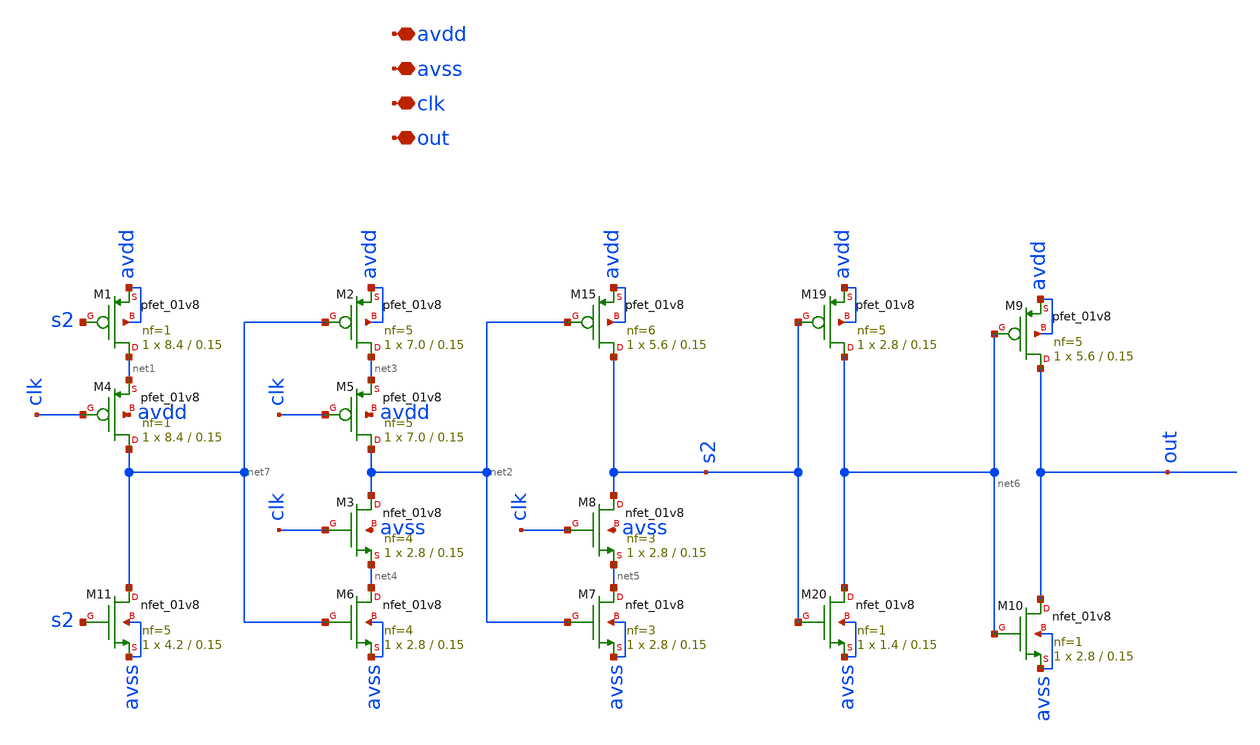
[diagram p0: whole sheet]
** sch_path: xschem/d_ff_2.sch
**.subckt d_ff_2 avdd avss clk out
*.iopin avdd
*.iopin avss
*.iopin clk
*.iopin out
XM4 net7 clk net1 avdd sky130_fd_pr__pfet_01v8 L=0.15 W=8.4 nf=1 ad='int((nf+1)/2) * W/nf * 0.29' as='int((nf+2)/2) * W/nf * 0.29'
+ pd='2*int((nf+1)/2) * (W/nf + 0.29)' ps='2*int((nf+2)/2) * (W/nf + 0.29)' nrd='0.29 / W' nrs='0.29 / W'
+ sa=0 sb=0 sd=0 mult=1 m=1
XM1 net1 s2 avdd avdd sky130_fd_pr__pfet_01v8 L=0.15 W=8.4 nf=1 ad='int((nf+1)/2) * W/nf * 0.29' as='int((nf+2)/2) * W/nf * 0.29'
+ pd='2*int((nf+1)/2) * (W/nf + 0.29)' ps='2*int((nf+2)/2) * (W/nf + 0.29)' nrd='0.29 / W' nrs='0.29 / W'
+ sa=0 sb=0 sd=0 mult=1 m=1
XM11 net7 s2 avss avss sky130_fd_pr__nfet_01v8 L=0.15 W=4.2 nf=5 ad='int((nf+1)/2) * W/nf * 0.29' as='int((nf+2)/2) * W/nf * 0.29'
+ pd='2*int((nf+1)/2) * (W/nf + 0.29)' ps='2*int((nf+2)/2) * (W/nf + 0.29)' nrd='0.29 / W' nrs='0.29 / W'
+ sa=0 sb=0 sd=0 mult=1 m=1
XM3 net2 clk net4 avss sky130_fd_pr__nfet_01v8 L=0.15 W=2.8 nf=4 ad='int((nf+1)/2) * W/nf * 0.29' as='int((nf+2)/2) * W/nf * 0.29'
+ pd='2*int((nf+1)/2) * (W/nf + 0.29)' ps='2*int((nf+2)/2) * (W/nf + 0.29)' nrd='0.29 / W' nrs='0.29 / W'
+ sa=0 sb=0 sd=0 mult=1 m=1
XM5 net2 clk net3 avdd sky130_fd_pr__pfet_01v8 L=0.15 W=7.0 nf=5 ad='int((nf+1)/2) * W/nf * 0.29' as='int((nf+2)/2) * W/nf * 0.29'
+ pd='2*int((nf+1)/2) * (W/nf + 0.29)' ps='2*int((nf+2)/2) * (W/nf + 0.29)' nrd='0.29 / W' nrs='0.29 / W'
+ sa=0 sb=0 sd=0 mult=1 m=1
XM2 net3 net7 avdd avdd sky130_fd_pr__pfet_01v8 L=0.15 W=7.0 nf=5 ad='int((nf+1)/2) * W/nf * 0.29' as='int((nf+2)/2) * W/nf * 0.29'
+ pd='2*int((nf+1)/2) * (W/nf + 0.29)' ps='2*int((nf+2)/2) * (W/nf + 0.29)' nrd='0.29 / W' nrs='0.29 / W'
+ sa=0 sb=0 sd=0 mult=1 m=1
XM6 net4 net7 avss avss sky130_fd_pr__nfet_01v8 L=0.15 W=2.8 nf=4 ad='int((nf+1)/2) * W/nf * 0.29' as='int((nf+2)/2) * W/nf * 0.29'
+ pd='2*int((nf+1)/2) * (W/nf + 0.29)' ps='2*int((nf+2)/2) * (W/nf + 0.29)' nrd='0.29 / W' nrs='0.29 / W'
+ sa=0 sb=0 sd=0 mult=1 m=1
XM8 s2 clk net5 avss sky130_fd_pr__nfet_01v8 L=0.15 W=2.8 nf=3 ad='int((nf+1)/2) * W/nf * 0.29' as='int((nf+2)/2) * W/nf * 0.29'
+ pd='2*int((nf+1)/2) * (W/nf + 0.29)' ps='2*int((nf+2)/2) * (W/nf + 0.29)' nrd='0.29 / W' nrs='0.29 / W'
+ sa=0 sb=0 sd=0 mult=1 m=1
XM15 s2 net2 avdd avdd sky130_fd_pr__pfet_01v8 L=0.15 W=5.6 nf=6 ad='int((nf+1)/2) * W/nf * 0.29' as='int((nf+2)/2) * W/nf * 0.29'
+ pd='2*int((nf+1)/2) * (W/nf + 0.29)' ps='2*int((nf+2)/2) * (W/nf + 0.29)' nrd='0.29 / W' nrs='0.29 / W'
+ sa=0 sb=0 sd=0 mult=1 m=1
XM7 net5 net2 avss avss sky130_fd_pr__nfet_01v8 L=0.15 W=2.8 nf=3 ad='int((nf+1)/2) * W/nf * 0.29' as='int((nf+2)/2) * W/nf * 0.29'
+ pd='2*int((nf+1)/2) * (W/nf + 0.29)' ps='2*int((nf+2)/2) * (W/nf + 0.29)' nrd='0.29 / W' nrs='0.29 / W'
+ sa=0 sb=0 sd=0 mult=1 m=1
XM19 net6 s2 avdd avdd sky130_fd_pr__pfet_01v8 L=0.15 W=2.8 nf=5 ad='int((nf+1)/2) * W/nf * 0.29' as='int((nf+2)/2) * W/nf * 0.29'
+ pd='2*int((nf+1)/2) * (W/nf + 0.29)' ps='2*int((nf+2)/2) * (W/nf + 0.29)' nrd='0.29 / W' nrs='0.29 / W'
+ sa=0 sb=0 sd=0 mult=1 m=1
XM20 net6 s2 avss avss sky130_fd_pr__nfet_01v8 L=0.15 W=1.4 nf=1 ad='int((nf+1)/2) * W/nf * 0.29' as='int((nf+2)/2) * W/nf * 0.29'
+ pd='2*int((nf+1)/2) * (W/nf + 0.29)' ps='2*int((nf+2)/2) * (W/nf + 0.29)' nrd='0.29 / W' nrs='0.29 / W'
+ sa=0 sb=0 sd=0 mult=1 m=1
XM9 out net6 avdd avdd sky130_fd_pr__pfet_01v8 L=0.15 W=5.6 nf=5 ad='int((nf+1)/2) * W/nf * 0.29' as='int((nf+2)/2) * W/nf * 0.29'
+ pd='2*int((nf+1)/2) * (W/nf + 0.29)' ps='2*int((nf+2)/2) * (W/nf + 0.29)' nrd='0.29 / W' nrs='0.29 / W'
+ sa=0 sb=0 sd=0 mult=1 m=1
XM10 out net6 avss avss sky130_fd_pr__nfet_01v8 L=0.15 W=2.8 nf=1 ad='int((nf+1)/2) * W/nf * 0.29' as='int((nf+2)/2) * W/nf * 0.29'
+ pd='2*int((nf+1)/2) * (W/nf + 0.29)' ps='2*int((nf+2)/2) * (W/nf + 0.29)' nrd='0.29 / W' nrs='0.29 / W'
+ sa=0 sb=0 sd=0 mult=1 m=1
**.ends
.end
